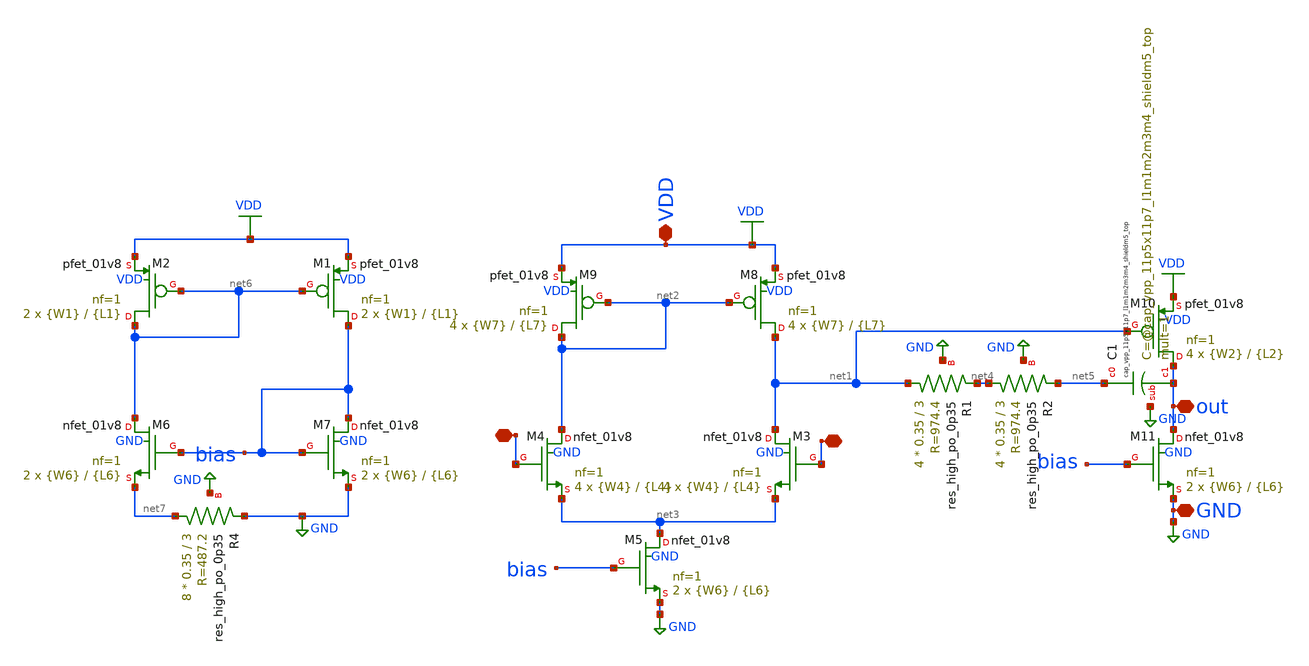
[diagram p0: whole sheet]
** sch_path: xschem/op5_exp.sch
**.subckt op5_exp GND - + VDD out
*.iopin GND
*.iopin -
*.iopin +
*.iopin VDD
*.iopin out
XM8 net1 net2 VDD VDD sky130_fd_pr__pfet_01v8 L={L7} W={W7} nf=1 ad='int((nf+1)/2) * W/nf * 0.29' as='int((nf+2)/2) * W/nf * 0.29'
+ pd='2*int((nf+1)/2) * (W/nf + 0.29)' ps='2*int((nf+2)/2) * (W/nf + 0.29)' nrd='0.29 / W' nrs='0.29 / W'
+ sa=0 sb=0 sd=0 mult=4 m=4
XM9 net2 net2 VDD VDD sky130_fd_pr__pfet_01v8 L={L7} W={W7} nf=1 ad='int((nf+1)/2) * W/nf * 0.29' as='int((nf+2)/2) * W/nf * 0.29'
+ pd='2*int((nf+1)/2) * (W/nf + 0.29)' ps='2*int((nf+2)/2) * (W/nf + 0.29)' nrd='0.29 / W' nrs='0.29 / W'
+ sa=0 sb=0 sd=0 mult=4 m=4
XM5 net3 bias GND GND sky130_fd_pr__nfet_01v8 L={L6} W={W6} nf=1 ad='int((nf+1)/2) * W/nf * 0.29' as='int((nf+2)/2) * W/nf * 0.29'
+ pd='2*int((nf+1)/2) * (W/nf + 0.29)' ps='2*int((nf+2)/2) * (W/nf + 0.29)' nrd='0.29 / W' nrs='0.29 / W'
+ sa=0 sb=0 sd=0 mult=2 m=2
XM10 out net1 VDD VDD sky130_fd_pr__pfet_01v8 L={L2} W={W2} nf=1 ad='int((nf+1)/2) * W/nf * 0.29' as='int((nf+2)/2) * W/nf * 0.29'
+ pd='2*int((nf+1)/2) * (W/nf + 0.29)' ps='2*int((nf+2)/2) * (W/nf + 0.29)' nrd='0.29 / W' nrs='0.29 / W'
+ sa=0 sb=0 sd=0 mult=4 m=4
XM11 out bias GND GND sky130_fd_pr__nfet_01v8 L={L6} W={W6} nf=1 ad='int((nf+1)/2) * W/nf * 0.29' as='int((nf+2)/2) * W/nf * 0.29'
+ pd='2*int((nf+1)/2) * (W/nf + 0.29)' ps='2*int((nf+2)/2) * (W/nf + 0.29)' nrd='0.29 / W' nrs='0.29 / W'
+ sa=0 sb=0 sd=0 mult=2 m=2
XM3 net1 + net3 GND sky130_fd_pr__nfet_01v8 L={L4} W={W4} nf=1 ad='int((nf+1)/2) * W/nf * 0.29' as='int((nf+2)/2) * W/nf * 0.29'
+ pd='2*int((nf+1)/2) * (W/nf + 0.29)' ps='2*int((nf+2)/2) * (W/nf + 0.29)' nrd='0.29 / W' nrs='0.29 / W'
+ sa=0 sb=0 sd=0 mult=4 m=4
XM1 bias net6 VDD VDD sky130_fd_pr__pfet_01v8 L={L1} W={W1} nf=1 ad='int((nf+1)/2) * W/nf * 0.29' as='int((nf+2)/2) * W/nf * 0.29'
+ pd='2*int((nf+1)/2) * (W/nf + 0.29)' ps='2*int((nf+2)/2) * (W/nf + 0.29)' nrd='0.29 / W' nrs='0.29 / W'
+ sa=0 sb=0 sd=0 mult=2 m=2
XM2 net6 net6 VDD VDD sky130_fd_pr__pfet_01v8 L={L1} W={W1} nf=1 ad='int((nf+1)/2) * W/nf * 0.29' as='int((nf+2)/2) * W/nf * 0.29'
+ pd='2*int((nf+1)/2) * (W/nf + 0.29)' ps='2*int((nf+2)/2) * (W/nf + 0.29)' nrd='0.29 / W' nrs='0.29 / W'
+ sa=0 sb=0 sd=0 mult=2 m=2
XM6 net6 bias net7 GND sky130_fd_pr__nfet_01v8 L={L6} W={W6} nf=1 ad='int((nf+1)/2) * W/nf * 0.29' as='int((nf+2)/2) * W/nf * 0.29'
+ pd='2*int((nf+1)/2) * (W/nf + 0.29)' ps='2*int((nf+2)/2) * (W/nf + 0.29)' nrd='0.29 / W' nrs='0.29 / W'
+ sa=0 sb=0 sd=0 mult=2 m=2
XM7 bias bias GND GND sky130_fd_pr__nfet_01v8 L={L6} W={W6} nf=1 ad='int((nf+1)/2) * W/nf * 0.29' as='int((nf+2)/2) * W/nf * 0.29'
+ pd='2*int((nf+1)/2) * (W/nf + 0.29)' ps='2*int((nf+2)/2) * (W/nf + 0.29)' nrd='0.29 / W' nrs='0.29 / W'
+ sa=0 sb=0 sd=0 mult=2 m=2
XR4 net7 GND GND sky130_fd_pr__res_high_po_0p35 L=3 mult=8 m=8
XM4 net2 - net3 GND sky130_fd_pr__nfet_01v8 L={L4} W={W4} nf=1 ad='int((nf+1)/2) * W/nf * 0.29' as='int((nf+2)/2) * W/nf * 0.29'
+ pd='2*int((nf+1)/2) * (W/nf + 0.29)' ps='2*int((nf+2)/2) * (W/nf + 0.29)' nrd='0.29 / W' nrs='0.29 / W'
+ sa=0 sb=0 sd=0 mult=4 m=4
XR1 net1 net4 GND sky130_fd_pr__res_high_po_0p35 L=3 mult=4 m=4
XR2 net4 net5 GND sky130_fd_pr__res_high_po_0p35 L=3 mult=4 m=4
XC1 net5 out GND sky130_fd_pr__cap_vpp_11p5x11p7_l1m1m2m3m4_shieldm5_top mult=1 m=1
**** begin user architecture code


**************
*PMOS cms
.param L1=20
.param W1=1
**************
*PMOS current differential
.param L7=10
.param W7=1

**************
*differential Pair
.param L4=10
.param W4=0.6

**************
*NMOS current control
.param L6=20
.param W6=1

**************
*Second Stage
.param L2=7
.param W2=1


**** end user architecture code
**.ends
.GLOBAL GND
.GLOBAL VDD
.end
